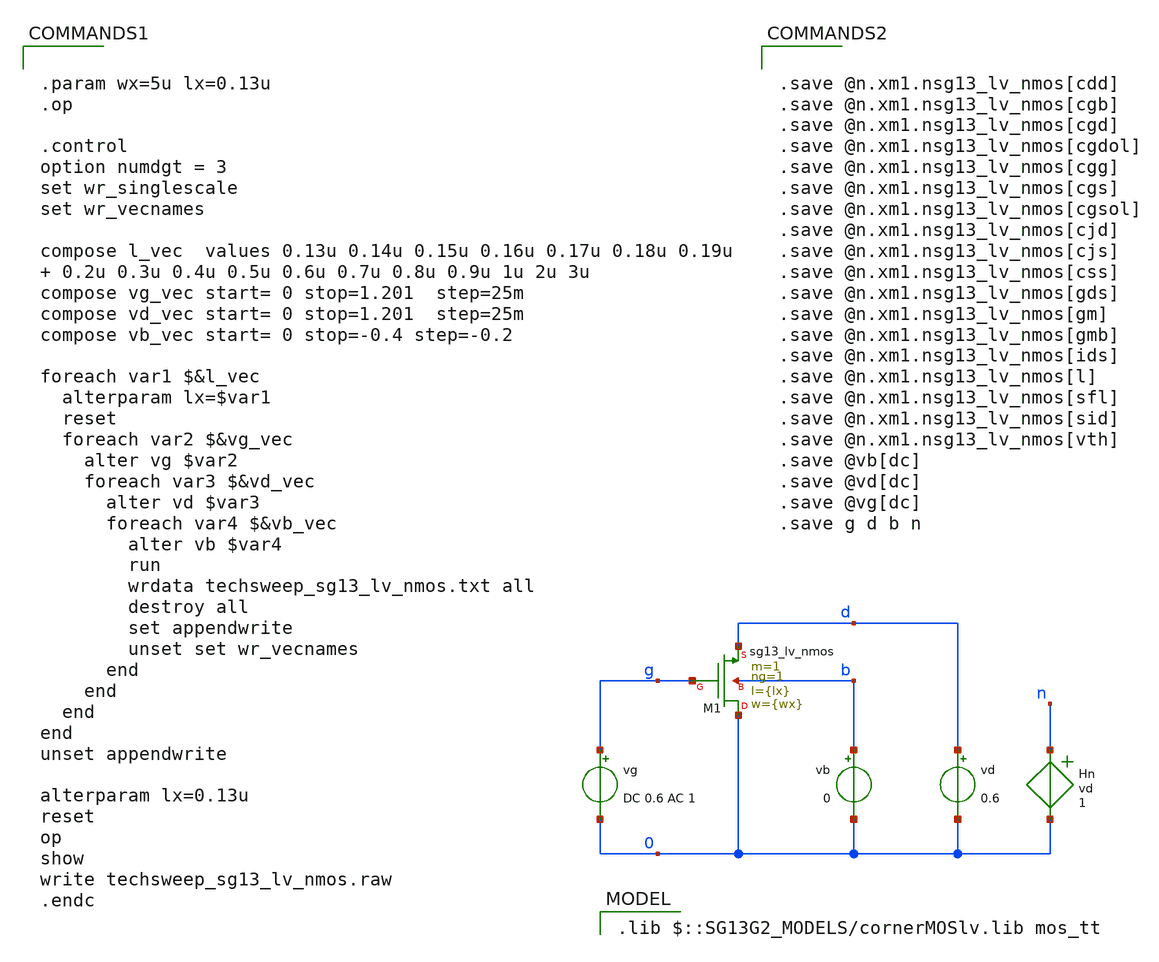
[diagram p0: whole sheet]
** sch_path: model/calculations/ihp-sg13g2_lookup/techsweep_sg13_lv_nmos.sch
**.subckt techsweep_sg13_lv_nmos
vg g 0 DC 0.6 AC 1
vd d 0 0.6
vb b 0 0
Hn n 0 vd 1
XM1 0 g d b sg13_lv_nmos w={wx} l={lx} ng=1 m=1 mm_ok=1
**** begin user architecture code


.param wx=5u lx=0.13u
.op

.control
option numdgt = 3
set wr_singlescale
set wr_vecnames

compose l_vec  values 0.13u 0.14u 0.15u 0.16u 0.17u 0.18u 0.19u  0.2u 0.3u 0.4u 0.5u 0.6u 0.7u 0.8u
+ 0.9u 1u 2u 3u
compose vg_vec start= 0 stop=1.201  step=25m
compose vd_vec start= 0 stop=1.201  step=25m
compose vb_vec start= 0 stop=-0.4 step=-0.2

foreach var1 $&l_vec
  alterparam lx=$var1
  reset
  foreach var2 $&vg_vec
    alter vg $var2
    foreach var3 $&vd_vec
      alter vd $var3
      foreach var4 $&vb_vec
        alter vb $var4
        run
        wrdata techsweep_sg13_lv_nmos.txt all
        destroy all
        set appendwrite
        unset set wr_vecnames
      end
    end
  end
end
unset appendwrite

alterparam lx=0.13u
reset
op
show
write techsweep_sg13_lv_nmos.raw
.endc




.save @n.xm1.nsg13_lv_nmos[cdd]
.save @n.xm1.nsg13_lv_nmos[cgb]
.save @n.xm1.nsg13_lv_nmos[cgd]
.save @n.xm1.nsg13_lv_nmos[cgdol]
.save @n.xm1.nsg13_lv_nmos[cgg]
.save @n.xm1.nsg13_lv_nmos[cgs]
.save @n.xm1.nsg13_lv_nmos[cgsol]
.save @n.xm1.nsg13_lv_nmos[cjd]
.save @n.xm1.nsg13_lv_nmos[cjs]
.save @n.xm1.nsg13_lv_nmos[css]
.save @n.xm1.nsg13_lv_nmos[gds]
.save @n.xm1.nsg13_lv_nmos[gm]
.save @n.xm1.nsg13_lv_nmos[gmb]
.save @n.xm1.nsg13_lv_nmos[ids]
.save @n.xm1.nsg13_lv_nmos[l]
.save @n.xm1.nsg13_lv_nmos[sfl]
.save @n.xm1.nsg13_lv_nmos[sid]
.save @n.xm1.nsg13_lv_nmos[vth]
.save @vb[dc]
.save @vd[dc]
.save @vg[dc]
.save g d b n


 .lib $::SG13G2_MODELS/cornerMOSlv.lib mos_tt
**** end user architecture code
**.ends
.end
